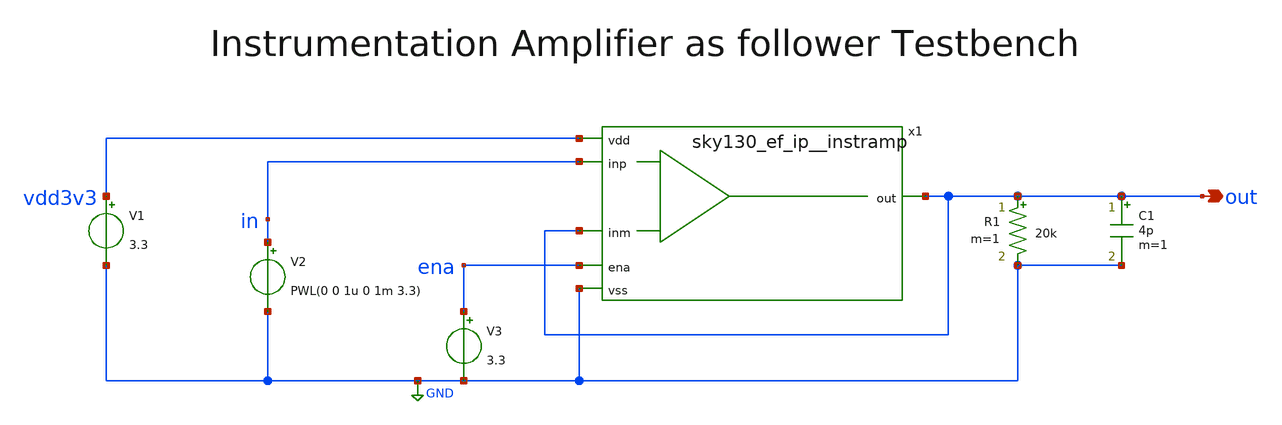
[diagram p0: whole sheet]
** sch_path: xschem/sky130_ef_ip__instramp_tb.sch
**.subckt sky130_ef_ip__instramp_tb out
*.opin out
V1 vdd3v3 GND 3.3
R1 out GND 20k m=1
V2 in GND PWL(0 0 1u 0 1m 3.3)
C1 out GND 4p m=1
x1 vdd3v3 out ena GND in out sky130_ef_ip__instramp
V3 ena GND 3.3
**** begin user architecture code

.lib /usr/share/pdk/sky130A/libs.tech/combined/sky130.lib.spice tt


.control
tran 100n 1.1m
plot V(out) V(in)
plot V(in) - V(out)
.endc

**** end user architecture code
**.ends
.GLOBAL GND
.end
